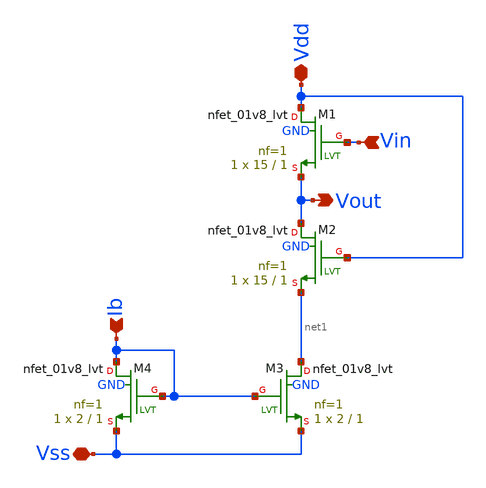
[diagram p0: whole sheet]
** sch_path: xschem/fvf.sch
**.subckt fvf Vin Ib Vout Vdd Vss
*.ipin Vin
*.ipin Ib
*.opin Vout
*.iopin Vdd
*.iopin Vss
XM1 Vdd Vin Vout GND sky130_fd_pr__nfet_01v8_lvt L=1 W=15 nf=1 ad='int((nf+1)/2) * W/nf * 0.29' as='int((nf+2)/2) * W/nf * 0.29'
+ pd='2*int((nf+1)/2) * (W/nf + 0.29)' ps='2*int((nf+2)/2) * (W/nf + 0.29)' nrd='0.29 / W' nrs='0.29 / W'
+ sa=0 sb=0 sd=0 mult=1 m=1
XM2 Vout Vdd net1 GND sky130_fd_pr__nfet_01v8_lvt L=1 W=15 nf=1 ad='int((nf+1)/2) * W/nf * 0.29' as='int((nf+2)/2) * W/nf * 0.29'
+ pd='2*int((nf+1)/2) * (W/nf + 0.29)' ps='2*int((nf+2)/2) * (W/nf + 0.29)' nrd='0.29 / W' nrs='0.29 / W'
+ sa=0 sb=0 sd=0 mult=1 m=1
XM3 net1 Ib Vss GND sky130_fd_pr__nfet_01v8_lvt L=1 W=2 nf=1 ad='int((nf+1)/2) * W/nf * 0.29' as='int((nf+2)/2) * W/nf * 0.29'
+ pd='2*int((nf+1)/2) * (W/nf + 0.29)' ps='2*int((nf+2)/2) * (W/nf + 0.29)' nrd='0.29 / W' nrs='0.29 / W'
+ sa=0 sb=0 sd=0 mult=1 m=1
XM4 Ib Ib Vss GND sky130_fd_pr__nfet_01v8_lvt L=1 W=2 nf=1 ad='int((nf+1)/2) * W/nf * 0.29' as='int((nf+2)/2) * W/nf * 0.29'
+ pd='2*int((nf+1)/2) * (W/nf + 0.29)' ps='2*int((nf+2)/2) * (W/nf + 0.29)' nrd='0.29 / W' nrs='0.29 / W'
+ sa=0 sb=0 sd=0 mult=1 m=1
**.ends
.end
